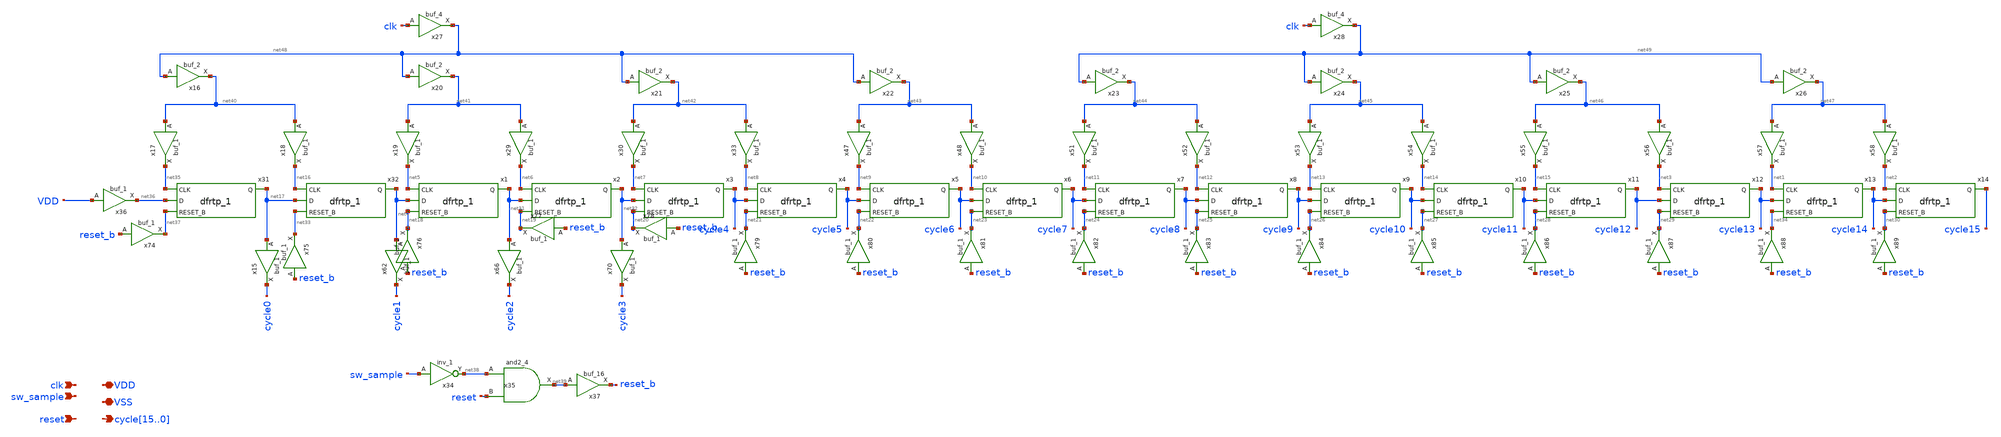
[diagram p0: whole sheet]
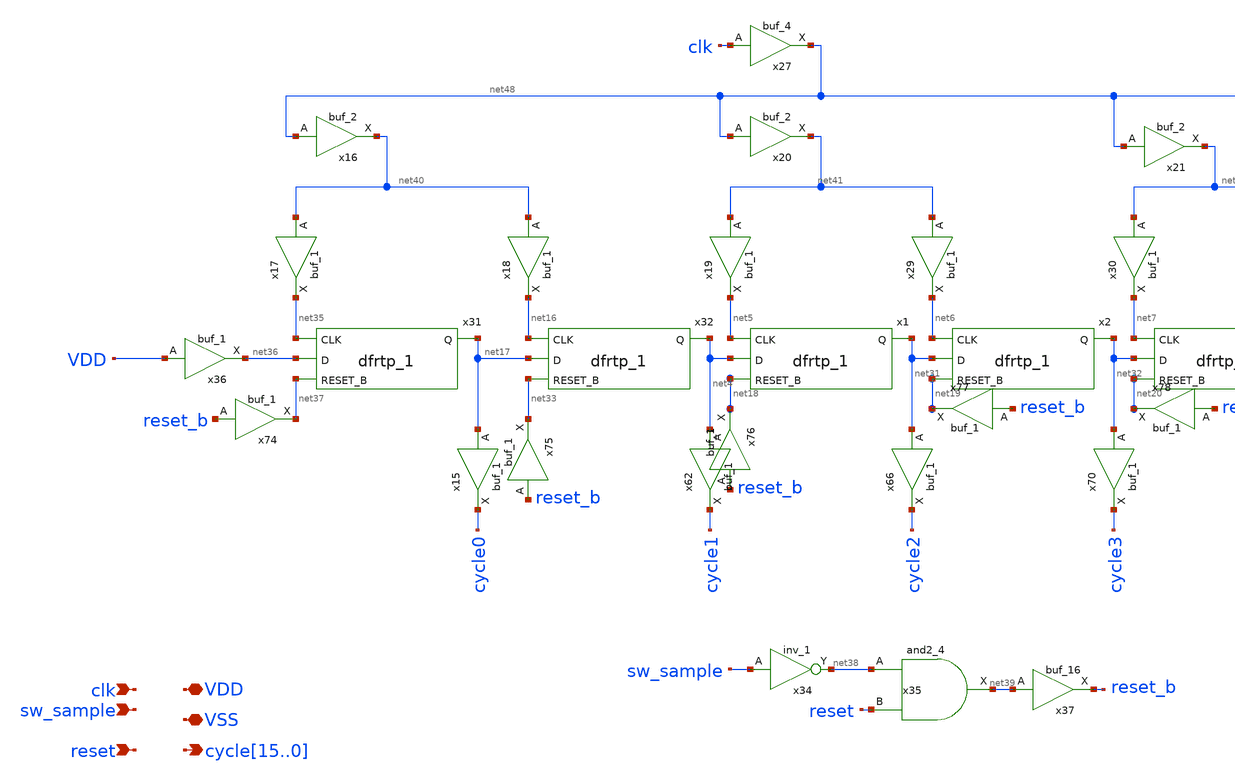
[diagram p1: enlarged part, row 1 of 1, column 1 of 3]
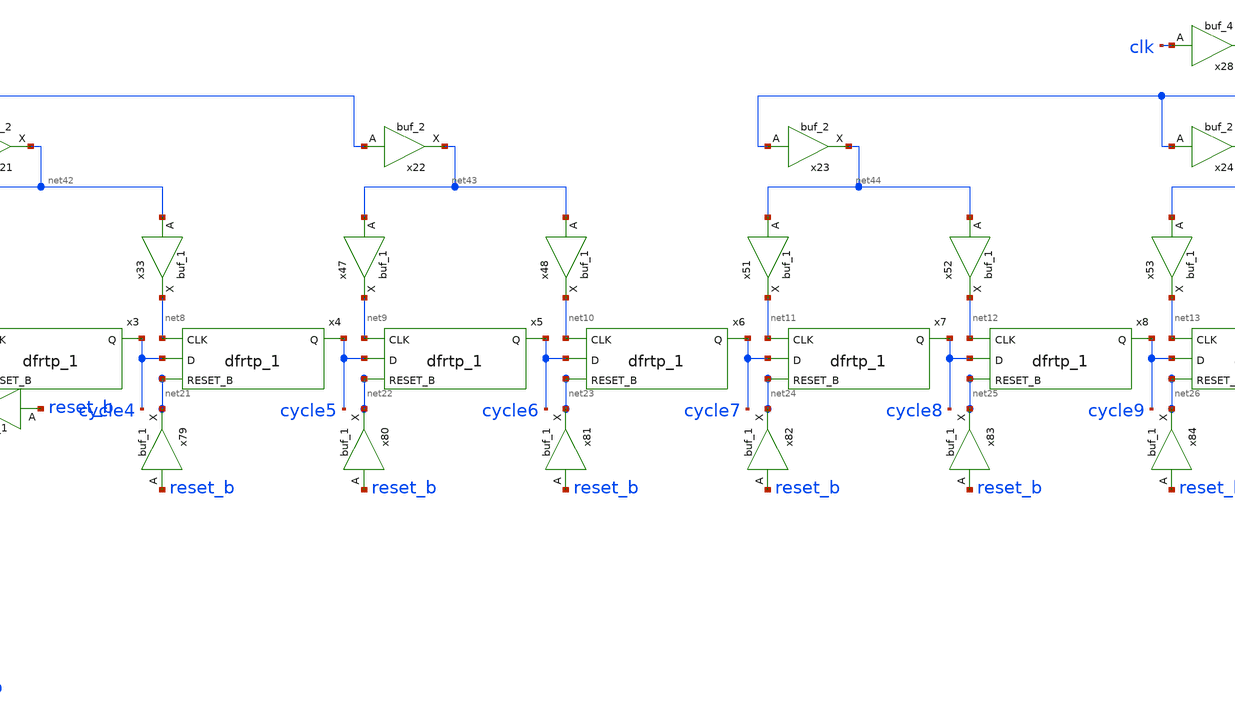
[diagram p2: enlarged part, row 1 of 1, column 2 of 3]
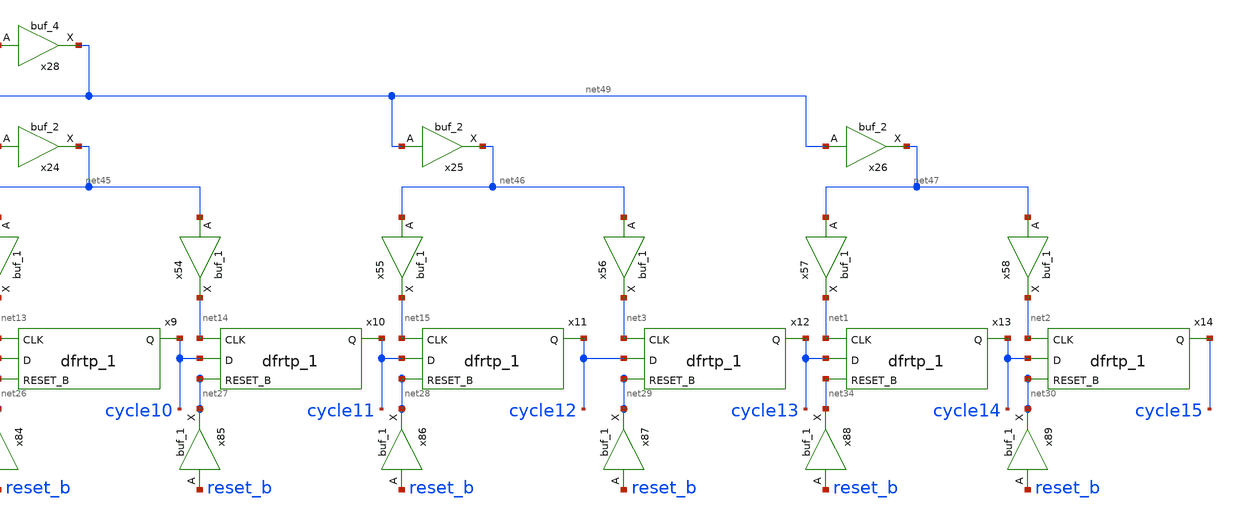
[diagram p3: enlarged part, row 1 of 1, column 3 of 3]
** sch_path: xschem/src/shifted_clock_generator/shifted_clock_generator.sch
**.subckt shifted_clock_generator
*+ cycle15,cycle14,cycle13,cycle12,cycle11,cycle10,cycle9,cycle8,cycle7,cycle6,cycle5,cycle4,cycle3,cycle2,cycle1,cycle0 VSS VDD clk reset sw_sample
*.opin
*+ cycle15,cycle14,cycle13,cycle12,cycle11,cycle10,cycle9,cycle8,cycle7,cycle6,cycle5,cycle4,cycle3,cycle2,cycle1,cycle0
*.iopin VSS
*.iopin VDD
*.ipin clk
*.ipin reset
*.ipin sw_sample
x32 net16 net17 net33 VSS VSS VDD VDD net4 sky130_fd_sc_hd__dfrtp_1
x1 net5 net4 net18 VSS VSS VDD VDD net31 sky130_fd_sc_hd__dfrtp_1
x2 net6 net31 net19 VSS VSS VDD VDD net32 sky130_fd_sc_hd__dfrtp_1
x3 net7 net32 net20 VSS VSS VDD VDD cycle4 sky130_fd_sc_hd__dfrtp_1
x4 net8 cycle4 net21 VSS VSS VDD VDD cycle5 sky130_fd_sc_hd__dfrtp_1
x5 net9 cycle5 net22 VSS VSS VDD VDD cycle6 sky130_fd_sc_hd__dfrtp_1
x6 net10 cycle6 net23 VSS VSS VDD VDD cycle7 sky130_fd_sc_hd__dfrtp_1
x7 net11 cycle7 net24 VSS VSS VDD VDD cycle8 sky130_fd_sc_hd__dfrtp_1
x8 net12 cycle8 net25 VSS VSS VDD VDD cycle9 sky130_fd_sc_hd__dfrtp_1
x9 net13 cycle9 net26 VSS VSS VDD VDD cycle10 sky130_fd_sc_hd__dfrtp_1
x10 net14 cycle10 net27 VSS VSS VDD VDD cycle11 sky130_fd_sc_hd__dfrtp_1
x11 net15 cycle11 net28 VSS VSS VDD VDD cycle12 sky130_fd_sc_hd__dfrtp_1
x12 net3 cycle12 net29 VSS VSS VDD VDD cycle13 sky130_fd_sc_hd__dfrtp_1
x13 net1 cycle13 net34 VSS VSS VDD VDD cycle14 sky130_fd_sc_hd__dfrtp_1
x14 net2 cycle14 net30 VSS VSS VDD VDD cycle15 sky130_fd_sc_hd__dfrtp_1
x31 net35 net36 net37 VSS VSS VDD VDD net17 sky130_fd_sc_hd__dfrtp_1
x37 net39 VSS VSS VDD VDD reset_b sky130_fd_sc_hd__buf_16
x35 net38 reset VSS VSS VDD VDD net39 sky130_fd_sc_hd__and2_4
x15 net17 VSS VSS VDD VDD cycle0 sky130_fd_sc_hd__buf_1
x16 net48 VSS VSS VDD VDD net40 sky130_fd_sc_hd__buf_2
x20 net48 VSS VSS VDD VDD net41 sky130_fd_sc_hd__buf_2
x21 net48 VSS VSS VDD VDD net42 sky130_fd_sc_hd__buf_2
x22 net48 VSS VSS VDD VDD net43 sky130_fd_sc_hd__buf_2
x23 net49 VSS VSS VDD VDD net44 sky130_fd_sc_hd__buf_2
x24 net49 VSS VSS VDD VDD net45 sky130_fd_sc_hd__buf_2
x25 net49 VSS VSS VDD VDD net46 sky130_fd_sc_hd__buf_2
x26 net49 VSS VSS VDD VDD net47 sky130_fd_sc_hd__buf_2
x27 clk VSS VSS VDD VDD net48 sky130_fd_sc_hd__buf_4
x28 clk VSS VSS VDD VDD net49 sky130_fd_sc_hd__buf_4
x17 net40 VSS VSS VDD VDD net35 sky130_fd_sc_hd__buf_1
x18 net40 VSS VSS VDD VDD net16 sky130_fd_sc_hd__buf_1
x19 net41 VSS VSS VDD VDD net5 sky130_fd_sc_hd__buf_1
x29 net41 VSS VSS VDD VDD net6 sky130_fd_sc_hd__buf_1
x30 net42 VSS VSS VDD VDD net7 sky130_fd_sc_hd__buf_1
x33 net42 VSS VSS VDD VDD net8 sky130_fd_sc_hd__buf_1
x47 net43 VSS VSS VDD VDD net9 sky130_fd_sc_hd__buf_1
x48 net43 VSS VSS VDD VDD net10 sky130_fd_sc_hd__buf_1
x51 net44 VSS VSS VDD VDD net11 sky130_fd_sc_hd__buf_1
x52 net44 VSS VSS VDD VDD net12 sky130_fd_sc_hd__buf_1
x53 net45 VSS VSS VDD VDD net13 sky130_fd_sc_hd__buf_1
x54 net45 VSS VSS VDD VDD net14 sky130_fd_sc_hd__buf_1
x55 net46 VSS VSS VDD VDD net15 sky130_fd_sc_hd__buf_1
x56 net46 VSS VSS VDD VDD net3 sky130_fd_sc_hd__buf_1
x57 net47 VSS VSS VDD VDD net1 sky130_fd_sc_hd__buf_1
x58 net47 VSS VSS VDD VDD net2 sky130_fd_sc_hd__buf_1
x62 net4 VSS VSS VDD VDD cycle1 sky130_fd_sc_hd__buf_1
x66 net31 VSS VSS VDD VDD cycle2 sky130_fd_sc_hd__buf_1
x70 net32 VSS VSS VDD VDD cycle3 sky130_fd_sc_hd__buf_1
x74 reset_b VSS VSS VDD VDD net37 sky130_fd_sc_hd__buf_1
x75 reset_b VSS VSS VDD VDD net33 sky130_fd_sc_hd__buf_1
x76 reset_b VSS VSS VDD VDD net18 sky130_fd_sc_hd__buf_1
x77 reset_b VSS VSS VDD VDD net19 sky130_fd_sc_hd__buf_1
x78 reset_b VSS VSS VDD VDD net20 sky130_fd_sc_hd__buf_1
x79 reset_b VSS VSS VDD VDD net21 sky130_fd_sc_hd__buf_1
x80 reset_b VSS VSS VDD VDD net22 sky130_fd_sc_hd__buf_1
x81 reset_b VSS VSS VDD VDD net23 sky130_fd_sc_hd__buf_1
x82 reset_b VSS VSS VDD VDD net24 sky130_fd_sc_hd__buf_1
x83 reset_b VSS VSS VDD VDD net25 sky130_fd_sc_hd__buf_1
x84 reset_b VSS VSS VDD VDD net26 sky130_fd_sc_hd__buf_1
x85 reset_b VSS VSS VDD VDD net27 sky130_fd_sc_hd__buf_1
x86 reset_b VSS VSS VDD VDD net28 sky130_fd_sc_hd__buf_1
x87 reset_b VSS VSS VDD VDD net29 sky130_fd_sc_hd__buf_1
x88 reset_b VSS VSS VDD VDD net34 sky130_fd_sc_hd__buf_1
x89 reset_b VSS VSS VDD VDD net30 sky130_fd_sc_hd__buf_1
x34 sw_sample VSS VSS VDD VDD net38 sky130_fd_sc_hd__inv_1
x36 VDD VSS VSS VDD VDD net36 sky130_fd_sc_hd__buf_1
**.ends
.end
